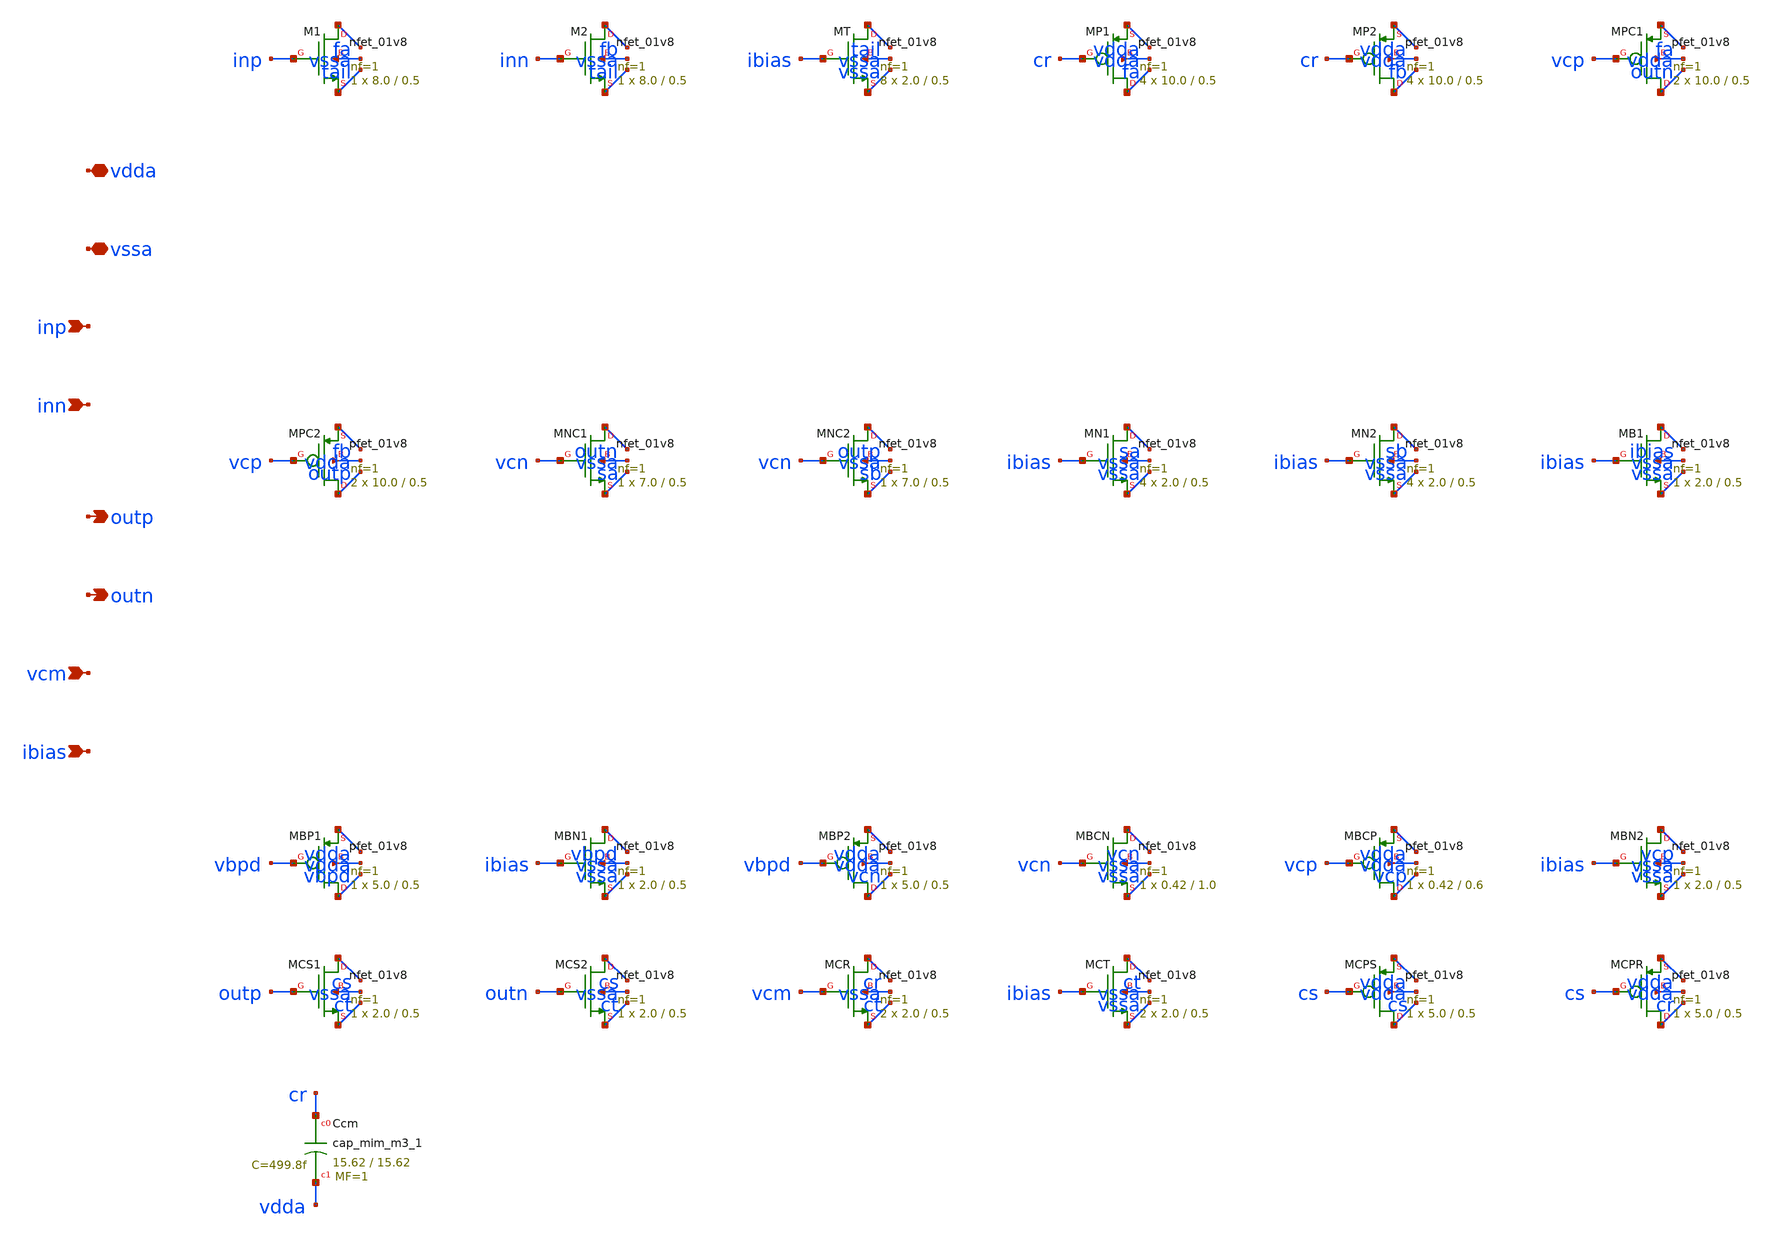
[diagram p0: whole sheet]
** sch_path: design/ota/ota_fd.sch
**.subckt ota_fd vdda vssa inp inn outp outn vcm ibias
*.iopin vdda
*.iopin vssa
*.ipin inp
*.ipin inn
*.opin outp
*.opin outn
*.ipin vcm
*.ipin ibias
XM1 fa inp tail vssa sky130_fd_pr__nfet_01v8 L=0.5 W=8.0 nf=1 ad='int((1 + 1)/2) * 8.0 / 1 * 0.29' as='int((1 + 2)/2) * 8.0 / 1 * 0.29'
+ pd='2*int((1 + 1)/2) * (8.0 / 1 + 0.29)' ps='2*int((1 + 2)/2) * (8.0 / 1 + 0.29)' nrd='0.29 / 8.0 ' nrs='0.29 / 8.0 '
+ sa=0 sb=0 sd=0 mult=1 m=1
XM2 fb inn tail vssa sky130_fd_pr__nfet_01v8 L=0.5 W=8.0 nf=1 ad='int((1 + 1)/2) * 8.0 / 1 * 0.29' as='int((1 + 2)/2) * 8.0 / 1 * 0.29'
+ pd='2*int((1 + 1)/2) * (8.0 / 1 + 0.29)' ps='2*int((1 + 2)/2) * (8.0 / 1 + 0.29)' nrd='0.29 / 8.0 ' nrs='0.29 / 8.0 '
+ sa=0 sb=0 sd=0 mult=1 m=1
XMT tail ibias vssa vssa sky130_fd_pr__nfet_01v8 L=0.5 W=2.0 nf=1 ad='int((1 + 1)/2) * 2.0 / 1 * 0.29'
+ as='int((1 + 2)/2) * 2.0 / 1 * 0.29' pd='2*int((1 + 1)/2) * (2.0 / 1 + 0.29)' ps='2*int((1 + 2)/2) * (2.0 / 1 + 0.29)'
+ nrd='0.29 / 2.0 ' nrs='0.29 / 2.0 ' sa=0 sb=0 sd=0 mult=8 m=8
XMP1 fa cr vdda vdda sky130_fd_pr__pfet_01v8 L=0.5 W=10.0 nf=1 ad='int((nf+1)/2) * W/nf * 0.29' as='int((nf+2)/2) * W/nf * 0.29'
+ pd='2*int((nf+1)/2) * (W/nf + 0.29)' ps='2*int((nf+2)/2) * (W/nf + 0.29)' nrd='0.29 / W' nrs='0.29 / W'
+ sa=0 sb=0 sd=0 mult=4 m=4
XMP2 fb cr vdda vdda sky130_fd_pr__pfet_01v8 L=0.5 W=10.0 nf=1 ad='int((nf+1)/2) * W/nf * 0.29' as='int((nf+2)/2) * W/nf * 0.29'
+ pd='2*int((nf+1)/2) * (W/nf + 0.29)' ps='2*int((nf+2)/2) * (W/nf + 0.29)' nrd='0.29 / W' nrs='0.29 / W'
+ sa=0 sb=0 sd=0 mult=4 m=4
XMPC1 outn vcp fa vdda sky130_fd_pr__pfet_01v8 L=0.5 W=10.0 nf=1 ad='int((nf+1)/2) * W/nf * 0.29' as='int((nf+2)/2) * W/nf * 0.29'
+ pd='2*int((nf+1)/2) * (W/nf + 0.29)' ps='2*int((nf+2)/2) * (W/nf + 0.29)' nrd='0.29 / W' nrs='0.29 / W'
+ sa=0 sb=0 sd=0 mult=2 m=2
XMPC2 outp vcp fb vdda sky130_fd_pr__pfet_01v8 L=0.5 W=10.0 nf=1 ad='int((nf+1)/2) * W/nf * 0.29' as='int((nf+2)/2) * W/nf * 0.29'
+ pd='2*int((nf+1)/2) * (W/nf + 0.29)' ps='2*int((nf+2)/2) * (W/nf + 0.29)' nrd='0.29 / W' nrs='0.29 / W'
+ sa=0 sb=0 sd=0 mult=2 m=2
XMNC1 outn vcn sa vssa sky130_fd_pr__nfet_01v8 L=0.5 W=7.0 nf=1 ad='int((1 + 1)/2) * 7.0 / 1 * 0.29'
+ as='int((1 + 2)/2) * 7.0 / 1 * 0.29' pd='2*int((1 + 1)/2) * (7.0 / 1 + 0.29)' ps='2*int((1 + 2)/2) * (7.0 / 1 + 0.29)'
+ nrd='0.29 / 7.0 ' nrs='0.29 / 7.0 ' sa=0 sb=0 sd=0 mult=1 m=1
XMNC2 outp vcn sb vssa sky130_fd_pr__nfet_01v8 L=0.5 W=7.0 nf=1 ad='int((1 + 1)/2) * 7.0 / 1 * 0.29'
+ as='int((1 + 2)/2) * 7.0 / 1 * 0.29' pd='2*int((1 + 1)/2) * (7.0 / 1 + 0.29)' ps='2*int((1 + 2)/2) * (7.0 / 1 + 0.29)'
+ nrd='0.29 / 7.0 ' nrs='0.29 / 7.0 ' sa=0 sb=0 sd=0 mult=1 m=1
XMN1 sa ibias vssa vssa sky130_fd_pr__nfet_01v8 L=0.5 W=2.0 nf=1 ad='int((1 + 1)/2) * 2.0 / 1 * 0.29'
+ as='int((1 + 2)/2) * 2.0 / 1 * 0.29' pd='2*int((1 + 1)/2) * (2.0 / 1 + 0.29)' ps='2*int((1 + 2)/2) * (2.0 / 1 + 0.29)'
+ nrd='0.29 / 2.0 ' nrs='0.29 / 2.0 ' sa=0 sb=0 sd=0 mult=4 m=4
XMN2 sb ibias vssa vssa sky130_fd_pr__nfet_01v8 L=0.5 W=2.0 nf=1 ad='int((1 + 1)/2) * 2.0 / 1 * 0.29'
+ as='int((1 + 2)/2) * 2.0 / 1 * 0.29' pd='2*int((1 + 1)/2) * (2.0 / 1 + 0.29)' ps='2*int((1 + 2)/2) * (2.0 / 1 + 0.29)'
+ nrd='0.29 / 2.0 ' nrs='0.29 / 2.0 ' sa=0 sb=0 sd=0 mult=4 m=4
XMB1 ibias ibias vssa vssa sky130_fd_pr__nfet_01v8 L=0.5 W=2.0 nf=1 ad='int((1 + 1)/2) * 2.0 / 1 * 0.29'
+ as='int((1 + 2)/2) * 2.0 / 1 * 0.29' pd='2*int((1 + 1)/2) * (2.0 / 1 + 0.29)' ps='2*int((1 + 2)/2) * (2.0 / 1 + 0.29)'
+ nrd='0.29 / 2.0 ' nrs='0.29 / 2.0 ' sa=0 sb=0 sd=0 mult=1 m=1
XMBP1 vbpd vbpd vdda vdda sky130_fd_pr__pfet_01v8 L=0.5 W=5.0 nf=1 ad='int((nf+1)/2) * W/nf * 0.29' as='int((nf+2)/2) * W/nf * 0.29'
+ pd='2*int((nf+1)/2) * (W/nf + 0.29)' ps='2*int((nf+2)/2) * (W/nf + 0.29)' nrd='0.29 / W' nrs='0.29 / W'
+ sa=0 sb=0 sd=0 mult=1 m=1
XMBN1 vbpd ibias vssa vssa sky130_fd_pr__nfet_01v8 L=0.5 W=2.0 nf=1 ad='int((1 + 1)/2) * 2.0 / 1 * 0.29'
+ as='int((1 + 2)/2) * 2.0 / 1 * 0.29' pd='2*int((1 + 1)/2) * (2.0 / 1 + 0.29)' ps='2*int((1 + 2)/2) * (2.0 / 1 + 0.29)'
+ nrd='0.29 / 2.0 ' nrs='0.29 / 2.0 ' sa=0 sb=0 sd=0 mult=1 m=1
XMBP2 vcn vbpd vdda vdda sky130_fd_pr__pfet_01v8 L=0.5 W=5.0 nf=1 ad='int((nf+1)/2) * W/nf * 0.29' as='int((nf+2)/2) * W/nf * 0.29'
+ pd='2*int((nf+1)/2) * (W/nf + 0.29)' ps='2*int((nf+2)/2) * (W/nf + 0.29)' nrd='0.29 / W' nrs='0.29 / W'
+ sa=0 sb=0 sd=0 mult=1 m=1
XMBCN vcn vcn vssa vssa sky130_fd_pr__nfet_01v8 L=1.0 W=0.42 nf=1 ad='int((1 + 1)/2) * 0.42 / 1 * 0.29'
+ as='int((1 + 2)/2) * 0.42 / 1 * 0.29' pd='2*int((1 + 1)/2) * (0.42 / 1 + 0.29)' ps='2*int((1 + 2)/2) * (0.42 / 1 + 0.29)'
+ nrd='0.29 / 0.42 ' nrs='0.29 / 0.42 ' sa=0 sb=0 sd=0 mult=1 m=1
XMBCP vcp vcp vdda vdda sky130_fd_pr__pfet_01v8 L=0.6 W=0.42 nf=1 ad='int((nf+1)/2) * W/nf * 0.29' as='int((nf+2)/2) * W/nf * 0.29'
+ pd='2*int((nf+1)/2) * (W/nf + 0.29)' ps='2*int((nf+2)/2) * (W/nf + 0.29)' nrd='0.29 / W' nrs='0.29 / W'
+ sa=0 sb=0 sd=0 mult=1 m=1
XMBN2 vcp ibias vssa vssa sky130_fd_pr__nfet_01v8 L=0.5 W=2.0 nf=1 ad='int((1 + 1)/2) * 2.0 / 1 * 0.29'
+ as='int((1 + 2)/2) * 2.0 / 1 * 0.29' pd='2*int((1 + 1)/2) * (2.0 / 1 + 0.29)' ps='2*int((1 + 2)/2) * (2.0 / 1 + 0.29)'
+ nrd='0.29 / 2.0 ' nrs='0.29 / 2.0 ' sa=0 sb=0 sd=0 mult=1 m=1
XMCS1 cs outp ct vssa sky130_fd_pr__nfet_01v8 L=0.5 W=2.0 nf=1 ad='int((1 + 1)/2) * 2.0 / 1 * 0.29' as='int((1 + 2)/2) * 2.0 / 1 * 0.29'
+ pd='2*int((1 + 1)/2) * (2.0 / 1 + 0.29)' ps='2*int((1 + 2)/2) * (2.0 / 1 + 0.29)' nrd='0.29 / 2.0 ' nrs='0.29 / 2.0 '
+ sa=0 sb=0 sd=0 mult=1 m=1
XMCS2 cs outn ct vssa sky130_fd_pr__nfet_01v8 L=0.5 W=2.0 nf=1 ad='int((1 + 1)/2) * 2.0 / 1 * 0.29' as='int((1 + 2)/2) * 2.0 / 1 * 0.29'
+ pd='2*int((1 + 1)/2) * (2.0 / 1 + 0.29)' ps='2*int((1 + 2)/2) * (2.0 / 1 + 0.29)' nrd='0.29 / 2.0 ' nrs='0.29 / 2.0 '
+ sa=0 sb=0 sd=0 mult=1 m=1
XMCR cr vcm ct vssa sky130_fd_pr__nfet_01v8 L=0.5 W=2.0 nf=1 ad='int((1 + 1)/2) * 2.0 / 1 * 0.29' as='int((1 + 2)/2) * 2.0 / 1 * 0.29'
+ pd='2*int((1 + 1)/2) * (2.0 / 1 + 0.29)' ps='2*int((1 + 2)/2) * (2.0 / 1 + 0.29)' nrd='0.29 / 2.0 ' nrs='0.29 / 2.0 '
+ sa=0 sb=0 sd=0 mult=2 m=2
XMCT ct ibias vssa vssa sky130_fd_pr__nfet_01v8 L=0.5 W=2.0 nf=1 ad='int((1 + 1)/2) * 2.0 / 1 * 0.29'
+ as='int((1 + 2)/2) * 2.0 / 1 * 0.29' pd='2*int((1 + 1)/2) * (2.0 / 1 + 0.29)' ps='2*int((1 + 2)/2) * (2.0 / 1 + 0.29)'
+ nrd='0.29 / 2.0 ' nrs='0.29 / 2.0 ' sa=0 sb=0 sd=0 mult=2 m=2
XMCPS cs cs vdda vdda sky130_fd_pr__pfet_01v8 L=0.5 W=5.0 nf=1 ad='int((nf+1)/2) * W/nf * 0.29' as='int((nf+2)/2) * W/nf * 0.29'
+ pd='2*int((nf+1)/2) * (W/nf + 0.29)' ps='2*int((nf+2)/2) * (W/nf + 0.29)' nrd='0.29 / W' nrs='0.29 / W'
+ sa=0 sb=0 sd=0 mult=1 m=1
XMCPR cr cs vdda vdda sky130_fd_pr__pfet_01v8 L=0.5 W=5.0 nf=1 ad='int((nf+1)/2) * W/nf * 0.29' as='int((nf+2)/2) * W/nf * 0.29'
+ pd='2*int((nf+1)/2) * (W/nf + 0.29)' ps='2*int((nf+2)/2) * (W/nf + 0.29)' nrd='0.29 / W' nrs='0.29 / W'
+ sa=0 sb=0 sd=0 mult=1 m=1
XCcm cr vdda sky130_fd_pr__cap_mim_m3_1 W=15.62 L=15.62 MF=1 m=1
**.ends
.end
